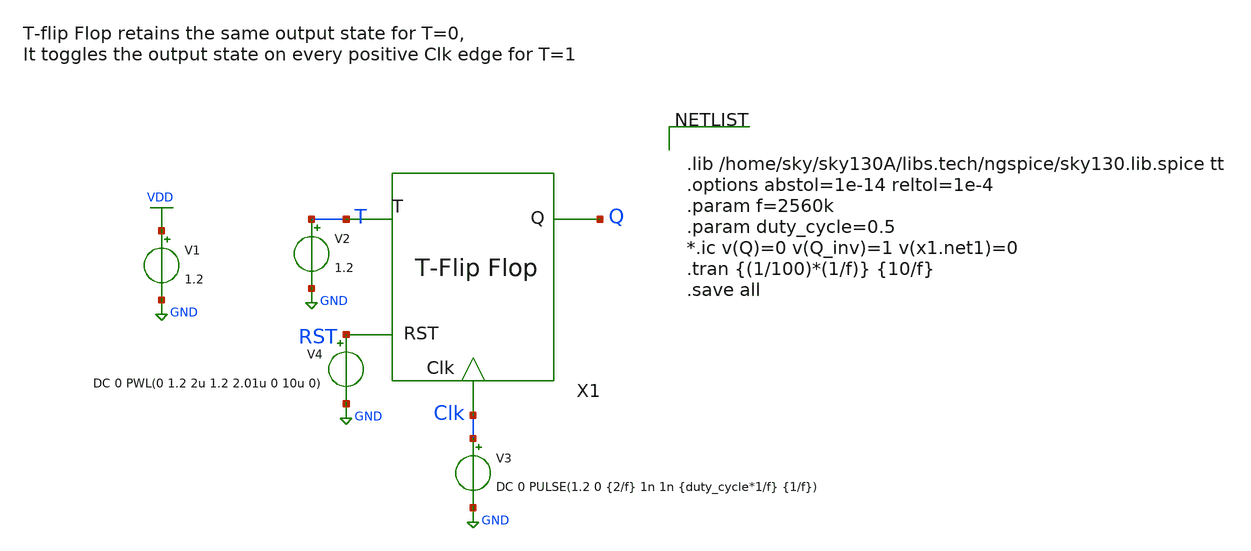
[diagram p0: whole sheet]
** sch_path: xschem/T_flip_flop/t_ff_rst_tb.sch
**.subckt t_ff_rst_tb
V1 VDD GND 1.2
V3 Clk GND DC 0 PULSE(1.2 0 {2/f} 1n 1n {duty_cycle*1/f} {1/f})
V2 T GND 1.2
X1 T Q Clk RST t_ff_rst
V4 RST GND DC 0 PWL(0 1.2 2u 1.2 2.01u 0 10u 0)
**** begin user architecture code


.lib /home/sky/sky130A/libs.tech/ngspice/sky130.lib.spice tt
.options abstol=1e-14 reltol=1e-4
.param f=2560k
.param duty_cycle=0.5
*.ic v(Q)=0 v(Q_inv)=1 v(x1.net1)=0
.tran {(1/100)*(1/f)} {10/f}
.save all


**** end user architecture code
**.ends

* expanding   symbol:  T_flip_flop/t_ff_rst.sym # of pins=4
** sym_path: xschem/T_flip_flop/t_ff_rst.sym
** sch_path: xschem/T_flip_flop/t_ff_rst.sch
.subckt t_ff_rst T Q Clk RST
*.ipin T
*.ipin Clk
*.opin Q
*.ipin RST
X2 Q T net1 exor_gate
X3 net1 Q Clk RST d_ff_rst
.ends


* expanding   symbol:  exor_gate/exor_gate.sym # of pins=3
** sym_path: xschem/exor_gate/exor_gate.sym
** sch_path: xschem/exor_gate/exor_gate.sch
.subckt exor_gate A B out
*.ipin A
*.ipin B
*.opin out
XM4 out A net1 GND sky130_fd_pr__nfet_01v8 L=0.18 W=0.5 nf=1 ad='int((nf+1)/2) * W/nf * 0.29' as='int((nf+2)/2) * W/nf * 0.29'
+ pd='2*int((nf+1)/2) * (W/nf + 0.29)' ps='2*int((nf+2)/2) * (W/nf + 0.29)' nrd='0.29 / W' nrs='0.29 / W'
+ sa=0 sb=0 sd=0 mult=1 m=1
XM5 net3 B VDD VDD sky130_fd_pr__pfet_01v8 L=0.18 W=1 nf=1 ad='int((nf+1)/2) * W/nf * 0.29' as='int((nf+2)/2) * W/nf * 0.29'
+ pd='2*int((nf+1)/2) * (W/nf + 0.29)' ps='2*int((nf+2)/2) * (W/nf + 0.29)' nrd='0.29 / W' nrs='0.29 / W'
+ sa=0 sb=0 sd=0 mult=1 m=1
XM1 net1 B GND GND sky130_fd_pr__nfet_01v8 L=0.18 W=0.5 nf=1 ad='int((nf+1)/2) * W/nf * 0.29' as='int((nf+2)/2) * W/nf * 0.29'
+ pd='2*int((nf+1)/2) * (W/nf + 0.29)' ps='2*int((nf+2)/2) * (W/nf + 0.29)' nrd='0.29 / W' nrs='0.29 / W'
+ sa=0 sb=0 sd=0 mult=1 m=1
XM2 out net5 net3 VDD sky130_fd_pr__pfet_01v8 L=0.18 W=1 nf=1 ad='int((nf+1)/2) * W/nf * 0.29' as='int((nf+2)/2) * W/nf * 0.29'
+ pd='2*int((nf+1)/2) * (W/nf + 0.29)' ps='2*int((nf+2)/2) * (W/nf + 0.29)' nrd='0.29 / W' nrs='0.29 / W'
+ sa=0 sb=0 sd=0 mult=1 m=1
XM3 net4 net6 VDD VDD sky130_fd_pr__pfet_01v8 L=0.18 W=1 nf=1 ad='int((nf+1)/2) * W/nf * 0.29' as='int((nf+2)/2) * W/nf * 0.29'
+ pd='2*int((nf+1)/2) * (W/nf + 0.29)' ps='2*int((nf+2)/2) * (W/nf + 0.29)' nrd='0.29 / W' nrs='0.29 / W'
+ sa=0 sb=0 sd=0 mult=1 m=1
XM6 out A net4 VDD sky130_fd_pr__pfet_01v8 L=0.18 W=1 nf=1 ad='int((nf+1)/2) * W/nf * 0.29' as='int((nf+2)/2) * W/nf * 0.29'
+ pd='2*int((nf+1)/2) * (W/nf + 0.29)' ps='2*int((nf+2)/2) * (W/nf + 0.29)' nrd='0.29 / W' nrs='0.29 / W'
+ sa=0 sb=0 sd=0 mult=1 m=1
XM7 out net5 net2 GND sky130_fd_pr__nfet_01v8 L=0.18 W=0.5 nf=1 ad='int((nf+1)/2) * W/nf * 0.29' as='int((nf+2)/2) * W/nf * 0.29'
+ pd='2*int((nf+1)/2) * (W/nf + 0.29)' ps='2*int((nf+2)/2) * (W/nf + 0.29)' nrd='0.29 / W' nrs='0.29 / W'
+ sa=0 sb=0 sd=0 mult=1 m=1
XM8 net2 net6 GND GND sky130_fd_pr__nfet_01v8 L=0.18 W=0.5 nf=1 ad='int((nf+1)/2) * W/nf * 0.29' as='int((nf+2)/2) * W/nf * 0.29'
+ pd='2*int((nf+1)/2) * (W/nf + 0.29)' ps='2*int((nf+2)/2) * (W/nf + 0.29)' nrd='0.29 / W' nrs='0.29 / W'
+ sa=0 sb=0 sd=0 mult=1 m=1
X3 B net6 inv Wpmos=3 Lpmos=0.18 Wnmos=1 Lnmos=0.18
X2 A net5 inv Wpmos=3 Lpmos=0.18 Wnmos=1 Lnmos=0.18
.ends


* expanding   symbol:  D_flip_flop/d_ff_rst.sym # of pins=4
** sym_path: xschem/D_flip_flop/d_ff_rst.sym
** sch_path: xschem/D_flip_flop/d_ff_rst.sch
.subckt d_ff_rst D Q Clk RST
*.ipin D
*.ipin Clk
*.opin Q
*.ipin RST
X1 net1 net2 inv Wpmos=3 Lpmos=0.18 Wnmos=1 Lnmos=0.18
X2 net3 Q inv Wpmos=3 Lpmos=0.18 Wnmos=1 Lnmos=0.18
X3 net2 net4 inv Wpmos=3 Lpmos=0.18 Wnmos=1 Lnmos=0.18
X4 Q net5 inv Wpmos=3 Lpmos=0.18 Wnmos=1 Lnmos=0.18
X5 net7 net1 Clk net6 transmission_gate Wpmos=1 Lpmos=0.18 Wnmos=1 Lnmos=0.18
X6 net1 net4 net6 Clk transmission_gate Wpmos=1 Lpmos=0.18 Wnmos=1 Lnmos=0.18
X7 net3 net5 Clk net6 transmission_gate Wpmos=1 Lpmos=0.18 Wnmos=1 Lnmos=0.18
X8 net2 net3 net6 Clk transmission_gate Wpmos=1 Lpmos=0.18 Wnmos=1 Lnmos=0.18
X9 Clk net6 inv Wpmos=3 Lpmos=0.18 Wnmos=1 Lnmos=0.18
X10 net8 D net7 and_gate
X11 RST net8 inv Wpmos=3 Lpmos=0.18 Wnmos=1 Lnmos=0.18
.ends


* expanding   symbol:  inv/inv.sym # of pins=2
** sym_path: xschem/inv/inv.sym
** sch_path: xschem/inv/inv.sch
.subckt inv in out  Wpmos=3 Lpmos=0.18 Wnmos=1 Lnmos=0.18
*.ipin in
*.iopin out
XM1 out in GND GND sky130_fd_pr__nfet_01v8 L=Lnmos W=Wnmos nf=1 ad='int((nf+1)/2) * W/nf * 0.29' as='int((nf+2)/2) * W/nf * 0.29'
+ pd='2*int((nf+1)/2) * (W/nf + 0.29)' ps='2*int((nf+2)/2) * (W/nf + 0.29)' nrd='0.29 / W' nrs='0.29 / W'
+ sa=0 sb=0 sd=0 mult=1 m=1
XM2 out in VDD VDD sky130_fd_pr__pfet_01v8 L=Lpmos W=Wpmos nf=1 ad='int((nf+1)/2) * W/nf * 0.29' as='int((nf+2)/2) * W/nf * 0.29'
+ pd='2*int((nf+1)/2) * (W/nf + 0.29)' ps='2*int((nf+2)/2) * (W/nf + 0.29)' nrd='0.29 / W' nrs='0.29 / W'
+ sa=0 sb=0 sd=0 mult=1 m=1
.ends


* expanding   symbol:  transmission_gate/transmission_gate.sym # of pins=4
** sym_path: xschem/transmission_gate/transmission_gate.sym
** sch_path: xschem/transmission_gate/transmission_gate.sch
.subckt transmission_gate in out ctrl_ ctrl  Wpmos=1 Lpmos=0.18 Wnmos=1 Lnmos=0.18
*.iopin in
*.iopin out
*.ipin ctrl_
*.ipin ctrl
XM1 in ctrl out GND sky130_fd_pr__nfet_01v8 L=Lnmos W=Wnmos nf=1 ad='int((nf+1)/2) * W/nf * 0.29' as='int((nf+2)/2) * W/nf * 0.29'
+ pd='2*int((nf+1)/2) * (W/nf + 0.29)' ps='2*int((nf+2)/2) * (W/nf + 0.29)' nrd='0.29 / W' nrs='0.29 / W'
+ sa=0 sb=0 sd=0 mult=1 m=1
XM2 out ctrl_ in VDD sky130_fd_pr__pfet_01v8 L=Lpmos W=Wpmos nf=1 ad='int((nf+1)/2) * W/nf * 0.29' as='int((nf+2)/2) * W/nf * 0.29'
+ pd='2*int((nf+1)/2) * (W/nf + 0.29)' ps='2*int((nf+2)/2) * (W/nf + 0.29)' nrd='0.29 / W' nrs='0.29 / W'
+ sa=0 sb=0 sd=0 mult=1 m=1
.ends


* expanding   symbol:  and_gate/and_gate.sym # of pins=3
** sym_path: xschem/and_gate/and_gate.sym
** sch_path: xschem/and_gate/and_gate.sch
.subckt and_gate A B out
*.ipin A
*.ipin B
*.opin out
XM1 net1 A net2 GND sky130_fd_pr__nfet_01v8 L=0.18 W=1 nf=1 ad='int((nf+1)/2) * W/nf * 0.29' as='int((nf+2)/2) * W/nf * 0.29'
+ pd='2*int((nf+1)/2) * (W/nf + 0.29)' ps='2*int((nf+2)/2) * (W/nf + 0.29)' nrd='0.29 / W' nrs='0.29 / W'
+ sa=0 sb=0 sd=0 mult=1 m=1
XM2 net1 A VDD VDD sky130_fd_pr__pfet_01v8 L=0.18 W=1 nf=1 ad='int((nf+1)/2) * W/nf * 0.29' as='int((nf+2)/2) * W/nf * 0.29'
+ pd='2*int((nf+1)/2) * (W/nf + 0.29)' ps='2*int((nf+2)/2) * (W/nf + 0.29)' nrd='0.29 / W' nrs='0.29 / W'
+ sa=0 sb=0 sd=0 mult=1 m=1
XM3 net1 B VDD VDD sky130_fd_pr__pfet_01v8 L=0.18 W=1 nf=1 ad='int((nf+1)/2) * W/nf * 0.29' as='int((nf+2)/2) * W/nf * 0.29'
+ pd='2*int((nf+1)/2) * (W/nf + 0.29)' ps='2*int((nf+2)/2) * (W/nf + 0.29)' nrd='0.29 / W' nrs='0.29 / W'
+ sa=0 sb=0 sd=0 mult=1 m=1
XM4 net2 B GND GND sky130_fd_pr__nfet_01v8 L=0.18 W=1 nf=1 ad='int((nf+1)/2) * W/nf * 0.29' as='int((nf+2)/2) * W/nf * 0.29'
+ pd='2*int((nf+1)/2) * (W/nf + 0.29)' ps='2*int((nf+2)/2) * (W/nf + 0.29)' nrd='0.29 / W' nrs='0.29 / W'
+ sa=0 sb=0 sd=0 mult=1 m=1
X1 net1 out inv Wpmos=3 Lpmos=0.18 Wnmos=1 Lnmos=0.18
.ends

.GLOBAL VDD
.GLOBAL GND
.end
